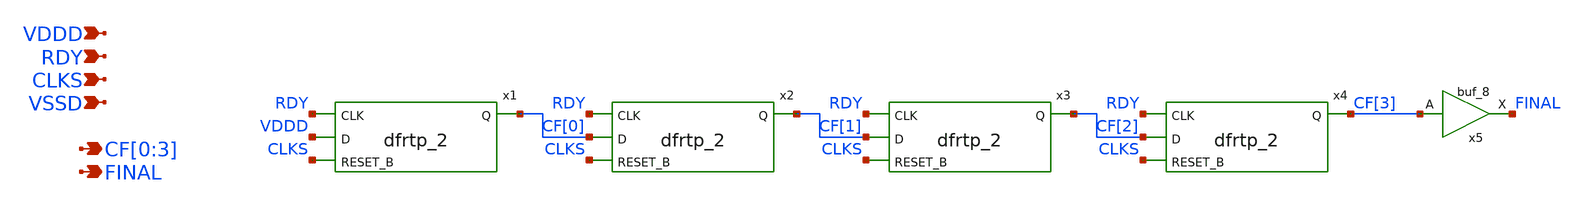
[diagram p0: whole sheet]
** sch_path: xschem/cyclic_flag.sch
**.subckt cyclic_flag RDY VDDD CLKS VSSD CF[0],CF[1],CF[2],CF[3] FINAL
*.ipin RDY
*.ipin VDDD
*.ipin CLKS
*.ipin VSSD
*.opin CF[0],CF[1],CF[2],CF[3]
*.opin FINAL
x1 RDY VDDD CLKS VSSD VSSD VDDD VDDD CF[0] sky130_fd_sc_hd__dfrtp_2
x2 RDY CF[0] CLKS VSSD VSSD VDDD VDDD CF[1] sky130_fd_sc_hd__dfrtp_2
x3 RDY CF[1] CLKS VSSD VSSD VDDD VDDD CF[2] sky130_fd_sc_hd__dfrtp_2
x4 RDY CF[2] CLKS VSSD VSSD VDDD VDDD CF[3] sky130_fd_sc_hd__dfrtp_2
x5 CF[3] VSSD VSSD VDDD VDDD FINAL sky130_fd_sc_hd__buf_8
**.ends
.end
